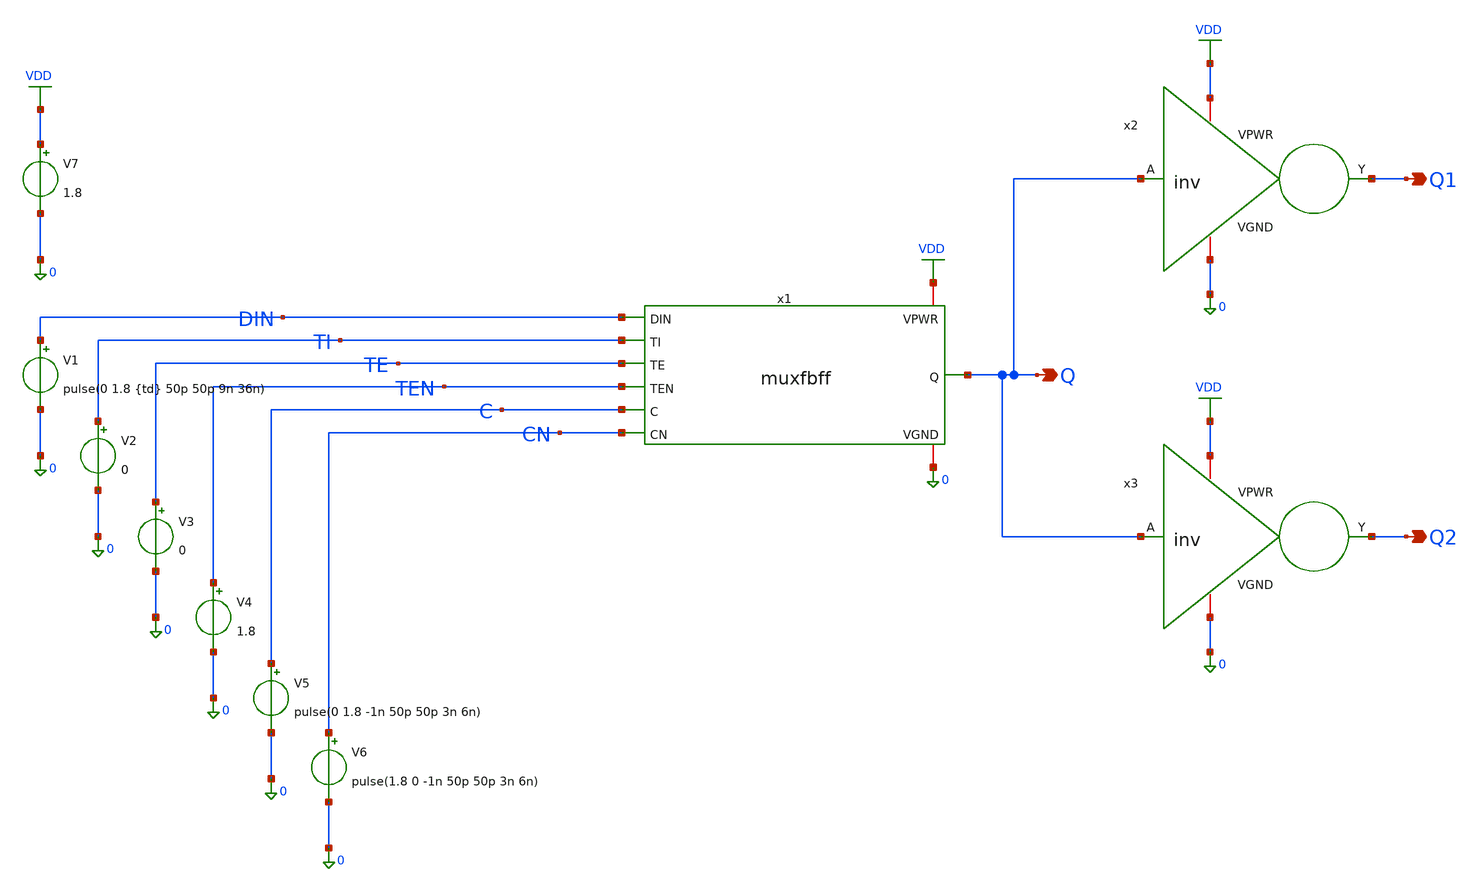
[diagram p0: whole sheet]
** sch_path: muxfbff/dataModefall/muxfbff_tb_datamode_fall_setup.sch
**.subckt muxfbff_tb_datamode_fall_setup Q Q1 Q2
*.opin Q
*.opin Q1
*.opin Q2
V1 DIN 0 pulse(0 1.8 {td} 50p 50p 9n 36n)
V2 TI 0 0
V3 TE 0 0
V4 TEN 0 1.8
V5 C 0 pulse(0 1.8 -1n 50p 50p 3n 6n)
V6 CN 0 pulse(1.8 0 -1n 50p 50p 3n 6n)
V7 VDD 0 1.8
x2 VDD Q Q1 0 inv
x3 VDD Q Q2 0 inv
x1 VDD 0 Q DIN TI TE TEN C CN muxfbff
**** begin user architecture code

** opencircuitdesign pdks install
.lib $::SKYWATER_MODELS/sky130.lib.spice tt




.tran 0.01n 20n
.param td = 0n

.control
  save all
  set filetype=ascii
  shell rm -f /home/sushanth/Desktop/HighSpeedScanFlop/muxfbff/dataModefall/delay.txt

  echo td,delay > /home/sushanth/Desktop/HighSpeedScanFlop/muxfbff/dataModefall/delay.txt

  let td = 0.33n
  let step = 1p

  while td <= 1.21n

    alterparam td = $&td
    let tdval = td     ; <-- KEY FIX

    reset
    run

    meas tran delay TRIG v(C) VAL=0.9 RISE=2 TARG v(Q) VAL=0.9 FALL=1

    print tdval,delay > /home/sushanth/Desktop/HighSpeedScanFlop/muxfbff/dataModefall/delay.txt


    let td = td + step

  end

.endc



**** end user architecture code
**.ends
.GLOBAL VDD
.end
